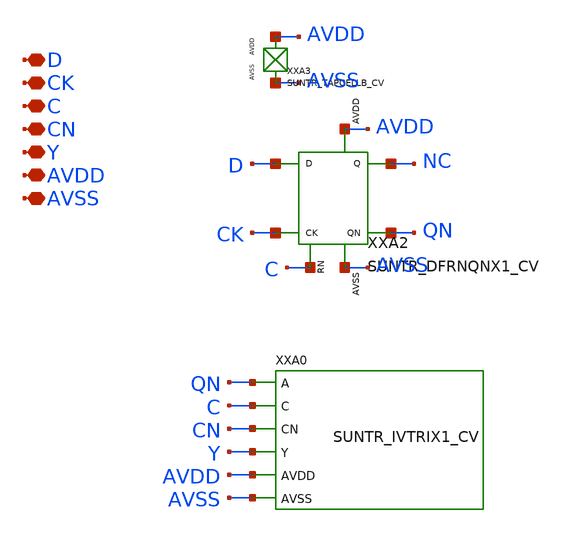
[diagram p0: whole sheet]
** sch_path: ip/sun_tr_sky130nm/design/SUN_TR_SKY130NM/SUNTR_DFTRIX1_CV.sch
**.subckt SUNTR_DFTRIX1_CV D CK C CN Y AVDD AVSS
*.iopin D
*.iopin CK
*.iopin C
*.iopin CN
*.iopin Y
*.iopin AVDD
*.iopin AVSS
XXA3 AVDD AVSS SUNTR_TAPCELLB_CV xoffset=0 yoffset=0 angle=0 M=1
XXA2 D CK C NC QN AVDD AVSS SUNTR_DFRNQNX1_CV xoffset=0 yoffset=0 angle=0
XXA0 QN C CN Y AVDD AVSS SUNTR_IVTRIX1_CV xoffset=0 yoffset=0 angle=0
**.ends
.end
